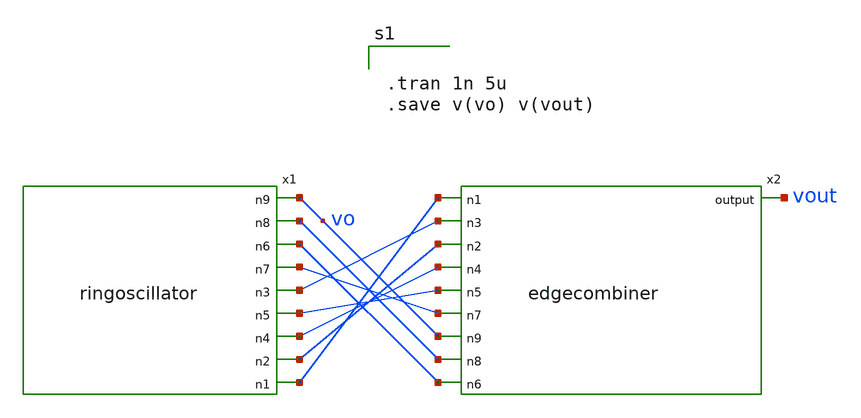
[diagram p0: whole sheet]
** sch_path: osccombiner.sch
**.subckt osccombiner
x2 vout net1 net3 net2 net4 net5 net7 vo net8 net6 edgecombiner
x1 vo net8 net6 net7 net3 net5 net4 net2 net1 ringoscillator
**** begin user architecture code


.tran 1n 5u
.save v(vo) v(vout)


*.lib ~/open_pdks/sky130/sky130A/libs.tech/ngspice/sky130.lib.spice tt
.param mc_mm_switch=0
.param mc_pr_switch=0

.include ~/open_pdks/sky130/sky130A/libs.tech/ngspice/corners/tt/nonfet.spice


*model
.include ~/open_pdks/sky130/sky130A/libs.tech/ngspice/all.spice

*mosfet
.include ~/open_pdks/sky130/sky130A/libs.ref/sky130_fd_pr/spice/sky130_fd_pr__pfet_01v8__tt.corner.spice
.inclued ~/open_pdks/sky130/sky130A/libs.ref/sky130_fd_pr/spice/sky130_fd_pr__nfet_01v8__tt.corner.spice

*mismatch parameters
.include ~/open_pdks/sky130/sky130A/libs.ref/sky130_fd_pr/spice/sky130_fd_pr__pfet_01v8__mismatch.corner.spice
.include ~/open_pdks/sky130/sky130A/libs.ref/sky130_fd_pr/spice/sky130_fd_pr__nfet_01v8__mismatch.corner.spice

**** end user architecture code
**.ends

* expanding   symbol:  /home/cegrahul/Downloads/edgecombiner.sym # of pins=10
** sym_path: edgecombiner.sym
** sch_path: edgecombiner.sch
.subckt edgecombiner output n1 n3 n2 n4 n5 n7 n9 n8 n6
*.ipin n1
*.ipin n2
*.ipin n3
*.ipin n4
*.ipin n5
*.ipin n6
*.ipin n7
*.ipin n8
*.ipin n9
*.opin output
XM3 v4 n5 VDD VDD sky130_fd_pr__pfet_01v8 L=0.15 W=1.68 nf=1 ad='int((nf+1)/2) * W/nf * 0.29' as='int((nf+2)/2) * W/nf * 0.29'
+ pd='2*int((nf+1)/2) * (W/nf + 0.29)' ps='2*int((nf+2)/2) * (W/nf + 0.29)' nrd='0.29 / W' nrs='0.29 / W'
+ sa=0 sb=0 sd=0 mult=1 m=1
XM4 v4 n4 VDD VDD sky130_fd_pr__pfet_01v8 L=0.15 W=1.68 nf=1 ad='int((nf+1)/2) * W/nf * 0.29' as='int((nf+2)/2) * W/nf * 0.29'
+ pd='2*int((nf+1)/2) * (W/nf + 0.29)' ps='2*int((nf+2)/2) * (W/nf + 0.29)' nrd='0.29 / W' nrs='0.29 / W'
+ sa=0 sb=0 sd=0 mult=1 m=1
XM5 v5 n5 net2 GND sky130_fd_pr__nfet_01v8 L=0.15 W=0.74 nf=1 ad='int((nf+1)/2) * W/nf * 0.29' as='int((nf+2)/2) * W/nf * 0.29'
+ pd='2*int((nf+1)/2) * (W/nf + 0.29)' ps='2*int((nf+2)/2) * (W/nf + 0.29)' nrd='0.29 / W' nrs='0.29 / W'
+ sa=0 sb=0 sd=0 mult=1 m=1
XM6 net2 n6 GND GND sky130_fd_pr__nfet_01v8 L=0.15 W=0.74 nf=1 ad='int((nf+1)/2) * W/nf * 0.29' as='int((nf+2)/2) * W/nf * 0.29'
+ pd='2*int((nf+1)/2) * (W/nf + 0.29)' ps='2*int((nf+2)/2) * (W/nf + 0.29)' nrd='0.29 / W' nrs='0.29 / W'
+ sa=0 sb=0 sd=0 mult=1 m=1
XM7 v5 n6 VDD VDD sky130_fd_pr__pfet_01v8 L=0.15 W=1.68 nf=1 ad='int((nf+1)/2) * W/nf * 0.29' as='int((nf+2)/2) * W/nf * 0.29'
+ pd='2*int((nf+1)/2) * (W/nf + 0.29)' ps='2*int((nf+2)/2) * (W/nf + 0.29)' nrd='0.29 / W' nrs='0.29 / W'
+ sa=0 sb=0 sd=0 mult=1 m=1
XM8 v5 n5 VDD VDD sky130_fd_pr__pfet_01v8 L=0.15 W=1.68 nf=1 ad='int((nf+1)/2) * W/nf * 0.29' as='int((nf+2)/2) * W/nf * 0.29'
+ pd='2*int((nf+1)/2) * (W/nf + 0.29)' ps='2*int((nf+2)/2) * (W/nf + 0.29)' nrd='0.29 / W' nrs='0.29 / W'
+ sa=0 sb=0 sd=0 mult=1 m=1
XM9 v6 n6 net3 GND sky130_fd_pr__nfet_01v8 L=0.15 W=0.74 nf=1 ad='int((nf+1)/2) * W/nf * 0.29' as='int((nf+2)/2) * W/nf * 0.29'
+ pd='2*int((nf+1)/2) * (W/nf + 0.29)' ps='2*int((nf+2)/2) * (W/nf + 0.29)' nrd='0.29 / W' nrs='0.29 / W'
+ sa=0 sb=0 sd=0 mult=1 m=1
XM10 net3 n7 GND GND sky130_fd_pr__nfet_01v8 L=0.15 W=0.74 nf=1 ad='int((nf+1)/2) * W/nf * 0.29' as='int((nf+2)/2) * W/nf * 0.29'
+ pd='2*int((nf+1)/2) * (W/nf + 0.29)' ps='2*int((nf+2)/2) * (W/nf + 0.29)' nrd='0.29 / W' nrs='0.29 / W'
+ sa=0 sb=0 sd=0 mult=1 m=1
XM11 v6 n7 VDD VDD sky130_fd_pr__pfet_01v8 L=0.15 W=1.68 nf=1 ad='int((nf+1)/2) * W/nf * 0.29' as='int((nf+2)/2) * W/nf * 0.29'
+ pd='2*int((nf+1)/2) * (W/nf + 0.29)' ps='2*int((nf+2)/2) * (W/nf + 0.29)' nrd='0.29 / W' nrs='0.29 / W'
+ sa=0 sb=0 sd=0 mult=1 m=1
XM12 v6 n6 VDD VDD sky130_fd_pr__pfet_01v8 L=0.15 W=1.68 nf=1 ad='int((nf+1)/2) * W/nf * 0.29' as='int((nf+2)/2) * W/nf * 0.29'
+ pd='2*int((nf+1)/2) * (W/nf + 0.29)' ps='2*int((nf+2)/2) * (W/nf + 0.29)' nrd='0.29 / W' nrs='0.29 / W'
+ sa=0 sb=0 sd=0 mult=1 m=1
XM13 v7 n7 net4 GND sky130_fd_pr__nfet_01v8 L=0.15 W=0.74 nf=1 ad='int((nf+1)/2) * W/nf * 0.29' as='int((nf+2)/2) * W/nf * 0.29'
+ pd='2*int((nf+1)/2) * (W/nf + 0.29)' ps='2*int((nf+2)/2) * (W/nf + 0.29)' nrd='0.29 / W' nrs='0.29 / W'
+ sa=0 sb=0 sd=0 mult=1 m=1
XM14 net4 n8 GND GND sky130_fd_pr__nfet_01v8 L=0.15 W=0.74 nf=1 ad='int((nf+1)/2) * W/nf * 0.29' as='int((nf+2)/2) * W/nf * 0.29'
+ pd='2*int((nf+1)/2) * (W/nf + 0.29)' ps='2*int((nf+2)/2) * (W/nf + 0.29)' nrd='0.29 / W' nrs='0.29 / W'
+ sa=0 sb=0 sd=0 mult=1 m=1
XM15 v7 n8 VDD VDD sky130_fd_pr__pfet_01v8 L=0.15 W=1.68 nf=1 ad='int((nf+1)/2) * W/nf * 0.29' as='int((nf+2)/2) * W/nf * 0.29'
+ pd='2*int((nf+1)/2) * (W/nf + 0.29)' ps='2*int((nf+2)/2) * (W/nf + 0.29)' nrd='0.29 / W' nrs='0.29 / W'
+ sa=0 sb=0 sd=0 mult=1 m=1
XM16 v7 n7 VDD VDD sky130_fd_pr__pfet_01v8 L=0.15 W=1.68 nf=1 ad='int((nf+1)/2) * W/nf * 0.29' as='int((nf+2)/2) * W/nf * 0.29'
+ pd='2*int((nf+1)/2) * (W/nf + 0.29)' ps='2*int((nf+2)/2) * (W/nf + 0.29)' nrd='0.29 / W' nrs='0.29 / W'
+ sa=0 sb=0 sd=0 mult=1 m=1
XM17 v4 n4 net1 GND sky130_fd_pr__nfet_01v8 L=0.15 W=0.74 nf=1 ad='int((nf+1)/2) * W/nf * 0.29' as='int((nf+2)/2) * W/nf * 0.29'
+ pd='2*int((nf+1)/2) * (W/nf + 0.29)' ps='2*int((nf+2)/2) * (W/nf + 0.29)' nrd='0.29 / W' nrs='0.29 / W'
+ sa=0 sb=0 sd=0 mult=1 m=1
XM18 net1 n5 GND GND sky130_fd_pr__nfet_01v8 L=0.15 W=0.74 nf=1 ad='int((nf+1)/2) * W/nf * 0.29' as='int((nf+2)/2) * W/nf * 0.29'
+ pd='2*int((nf+1)/2) * (W/nf + 0.29)' ps='2*int((nf+2)/2) * (W/nf + 0.29)' nrd='0.29 / W' nrs='0.29 / W'
+ sa=0 sb=0 sd=0 mult=1 m=1
XM19 v4 n5 VDD VDD sky130_fd_pr__pfet_01v8 L=0.15 W=1.68 nf=1 ad='int((nf+1)/2) * W/nf * 0.29' as='int((nf+2)/2) * W/nf * 0.29'
+ pd='2*int((nf+1)/2) * (W/nf + 0.29)' ps='2*int((nf+2)/2) * (W/nf + 0.29)' nrd='0.29 / W' nrs='0.29 / W'
+ sa=0 sb=0 sd=0 mult=1 m=1
XM20 v4 n4 VDD VDD sky130_fd_pr__pfet_01v8 L=0.15 W=1.68 nf=1 ad='int((nf+1)/2) * W/nf * 0.29' as='int((nf+2)/2) * W/nf * 0.29'
+ pd='2*int((nf+1)/2) * (W/nf + 0.29)' ps='2*int((nf+2)/2) * (W/nf + 0.29)' nrd='0.29 / W' nrs='0.29 / W'
+ sa=0 sb=0 sd=0 mult=1 m=1
XM21 v8 n8 net5 GND sky130_fd_pr__nfet_01v8 L=0.15 W=0.74 nf=1 ad='int((nf+1)/2) * W/nf * 0.29' as='int((nf+2)/2) * W/nf * 0.29'
+ pd='2*int((nf+1)/2) * (W/nf + 0.29)' ps='2*int((nf+2)/2) * (W/nf + 0.29)' nrd='0.29 / W' nrs='0.29 / W'
+ sa=0 sb=0 sd=0 mult=1 m=1
XM22 net5 n9 GND GND sky130_fd_pr__nfet_01v8 L=0.15 W=0.74 nf=1 ad='int((nf+1)/2) * W/nf * 0.29' as='int((nf+2)/2) * W/nf * 0.29'
+ pd='2*int((nf+1)/2) * (W/nf + 0.29)' ps='2*int((nf+2)/2) * (W/nf + 0.29)' nrd='0.29 / W' nrs='0.29 / W'
+ sa=0 sb=0 sd=0 mult=1 m=1
XM23 v8 n9 VDD VDD sky130_fd_pr__pfet_01v8 L=0.15 W=1.68 nf=1 ad='int((nf+1)/2) * W/nf * 0.29' as='int((nf+2)/2) * W/nf * 0.29'
+ pd='2*int((nf+1)/2) * (W/nf + 0.29)' ps='2*int((nf+2)/2) * (W/nf + 0.29)' nrd='0.29 / W' nrs='0.29 / W'
+ sa=0 sb=0 sd=0 mult=1 m=1
XM24 v8 n8 VDD VDD sky130_fd_pr__pfet_01v8 L=0.15 W=1.68 nf=1 ad='int((nf+1)/2) * W/nf * 0.29' as='int((nf+2)/2) * W/nf * 0.29'
+ pd='2*int((nf+1)/2) * (W/nf + 0.29)' ps='2*int((nf+2)/2) * (W/nf + 0.29)' nrd='0.29 / W' nrs='0.29 / W'
+ sa=0 sb=0 sd=0 mult=1 m=1
XM25 v9 n9 net6 GND sky130_fd_pr__nfet_01v8 L=0.15 W=0.74 nf=1 ad='int((nf+1)/2) * W/nf * 0.29' as='int((nf+2)/2) * W/nf * 0.29'
+ pd='2*int((nf+1)/2) * (W/nf + 0.29)' ps='2*int((nf+2)/2) * (W/nf + 0.29)' nrd='0.29 / W' nrs='0.29 / W'
+ sa=0 sb=0 sd=0 mult=1 m=1
XM26 net6 n1 GND GND sky130_fd_pr__nfet_01v8 L=0.15 W=0.74 nf=1 ad='int((nf+1)/2) * W/nf * 0.29' as='int((nf+2)/2) * W/nf * 0.29'
+ pd='2*int((nf+1)/2) * (W/nf + 0.29)' ps='2*int((nf+2)/2) * (W/nf + 0.29)' nrd='0.29 / W' nrs='0.29 / W'
+ sa=0 sb=0 sd=0 mult=1 m=1
XM27 v9 n1 VDD VDD sky130_fd_pr__pfet_01v8 L=0.15 W=1.68 nf=1 ad='int((nf+1)/2) * W/nf * 0.29' as='int((nf+2)/2) * W/nf * 0.29'
+ pd='2*int((nf+1)/2) * (W/nf + 0.29)' ps='2*int((nf+2)/2) * (W/nf + 0.29)' nrd='0.29 / W' nrs='0.29 / W'
+ sa=0 sb=0 sd=0 mult=1 m=1
XM28 v9 n9 VDD VDD sky130_fd_pr__pfet_01v8 L=0.15 W=1.68 nf=1 ad='int((nf+1)/2) * W/nf * 0.29' as='int((nf+2)/2) * W/nf * 0.29'
+ pd='2*int((nf+1)/2) * (W/nf + 0.29)' ps='2*int((nf+2)/2) * (W/nf + 0.29)' nrd='0.29 / W' nrs='0.29 / W'
+ sa=0 sb=0 sd=0 mult=1 m=1
XM29 v3 n3 net7 GND sky130_fd_pr__nfet_01v8 L=0.15 W=0.74 nf=1 ad='int((nf+1)/2) * W/nf * 0.29' as='int((nf+2)/2) * W/nf * 0.29'
+ pd='2*int((nf+1)/2) * (W/nf + 0.29)' ps='2*int((nf+2)/2) * (W/nf + 0.29)' nrd='0.29 / W' nrs='0.29 / W'
+ sa=0 sb=0 sd=0 mult=1 m=1
XM30 net7 n4 GND GND sky130_fd_pr__nfet_01v8 L=0.15 W=0.74 nf=1 ad='int((nf+1)/2) * W/nf * 0.29' as='int((nf+2)/2) * W/nf * 0.29'
+ pd='2*int((nf+1)/2) * (W/nf + 0.29)' ps='2*int((nf+2)/2) * (W/nf + 0.29)' nrd='0.29 / W' nrs='0.29 / W'
+ sa=0 sb=0 sd=0 mult=1 m=1
XM31 v3 n4 VDD VDD sky130_fd_pr__pfet_01v8 L=0.15 W=1.68 nf=1 ad='int((nf+1)/2) * W/nf * 0.29' as='int((nf+2)/2) * W/nf * 0.29'
+ pd='2*int((nf+1)/2) * (W/nf + 0.29)' ps='2*int((nf+2)/2) * (W/nf + 0.29)' nrd='0.29 / W' nrs='0.29 / W'
+ sa=0 sb=0 sd=0 mult=1 m=1
XM32 v3 n3 VDD VDD sky130_fd_pr__pfet_01v8 L=0.15 W=1.68 nf=1 ad='int((nf+1)/2) * W/nf * 0.29' as='int((nf+2)/2) * W/nf * 0.29'
+ pd='2*int((nf+1)/2) * (W/nf + 0.29)' ps='2*int((nf+2)/2) * (W/nf + 0.29)' nrd='0.29 / W' nrs='0.29 / W'
+ sa=0 sb=0 sd=0 mult=1 m=1
XM33 v2 n2 net8 GND sky130_fd_pr__nfet_01v8 L=0.15 W=0.74 nf=1 ad='int((nf+1)/2) * W/nf * 0.29' as='int((nf+2)/2) * W/nf * 0.29'
+ pd='2*int((nf+1)/2) * (W/nf + 0.29)' ps='2*int((nf+2)/2) * (W/nf + 0.29)' nrd='0.29 / W' nrs='0.29 / W'
+ sa=0 sb=0 sd=0 mult=1 m=1
XM34 net8 n3 GND GND sky130_fd_pr__nfet_01v8 L=0.15 W=0.74 nf=1 ad='int((nf+1)/2) * W/nf * 0.29' as='int((nf+2)/2) * W/nf * 0.29'
+ pd='2*int((nf+1)/2) * (W/nf + 0.29)' ps='2*int((nf+2)/2) * (W/nf + 0.29)' nrd='0.29 / W' nrs='0.29 / W'
+ sa=0 sb=0 sd=0 mult=1 m=1
XM35 v2 n3 VDD VDD sky130_fd_pr__pfet_01v8 L=0.15 W=1.68 nf=1 ad='int((nf+1)/2) * W/nf * 0.29' as='int((nf+2)/2) * W/nf * 0.29'
+ pd='2*int((nf+1)/2) * (W/nf + 0.29)' ps='2*int((nf+2)/2) * (W/nf + 0.29)' nrd='0.29 / W' nrs='0.29 / W'
+ sa=0 sb=0 sd=0 mult=1 m=1
XM36 v2 n2 VDD VDD sky130_fd_pr__pfet_01v8 L=0.15 W=1.68 nf=1 ad='int((nf+1)/2) * W/nf * 0.29' as='int((nf+2)/2) * W/nf * 0.29'
+ pd='2*int((nf+1)/2) * (W/nf + 0.29)' ps='2*int((nf+2)/2) * (W/nf + 0.29)' nrd='0.29 / W' nrs='0.29 / W'
+ sa=0 sb=0 sd=0 mult=1 m=1
XM37 v1 n1 net9 GND sky130_fd_pr__nfet_01v8 L=0.15 W=0.74 nf=1 ad='int((nf+1)/2) * W/nf * 0.29' as='int((nf+2)/2) * W/nf * 0.29'
+ pd='2*int((nf+1)/2) * (W/nf + 0.29)' ps='2*int((nf+2)/2) * (W/nf + 0.29)' nrd='0.29 / W' nrs='0.29 / W'
+ sa=0 sb=0 sd=0 mult=1 m=1
XM38 net9 n2 GND GND sky130_fd_pr__nfet_01v8 L=0.15 W=0.74 nf=1 ad='int((nf+1)/2) * W/nf * 0.29' as='int((nf+2)/2) * W/nf * 0.29'
+ pd='2*int((nf+1)/2) * (W/nf + 0.29)' ps='2*int((nf+2)/2) * (W/nf + 0.29)' nrd='0.29 / W' nrs='0.29 / W'
+ sa=0 sb=0 sd=0 mult=1 m=1
XM39 v1 n2 VDD VDD sky130_fd_pr__pfet_01v8 L=0.15 W=1.68 nf=1 ad='int((nf+1)/2) * W/nf * 0.29' as='int((nf+2)/2) * W/nf * 0.29'
+ pd='2*int((nf+1)/2) * (W/nf + 0.29)' ps='2*int((nf+2)/2) * (W/nf + 0.29)' nrd='0.29 / W' nrs='0.29 / W'
+ sa=0 sb=0 sd=0 mult=1 m=1
XM40 v1 n1 VDD VDD sky130_fd_pr__pfet_01v8 L=0.15 W=1.68 nf=1 ad='int((nf+1)/2) * W/nf * 0.29' as='int((nf+2)/2) * W/nf * 0.29'
+ pd='2*int((nf+1)/2) * (W/nf + 0.29)' ps='2*int((nf+2)/2) * (W/nf + 0.29)' nrd='0.29 / W' nrs='0.29 / W'
+ sa=0 sb=0 sd=0 mult=1 m=1
V1 VDD GND 1.8
XM1 output v1 net10 GND sky130_fd_pr__nfet_01v8 L=0.15 W=0.74 nf=1 ad='int((nf+1)/2) * W/nf * 0.29' as='int((nf+2)/2) * W/nf * 0.29'
+ pd='2*int((nf+1)/2) * (W/nf + 0.29)' ps='2*int((nf+2)/2) * (W/nf + 0.29)' nrd='0.29 / W' nrs='0.29 / W'
+ sa=0 sb=0 sd=0 mult=1 m=1
XM2 net10 v2 net11 GND sky130_fd_pr__nfet_01v8 L=0.15 W=3 nf=1 ad='int((nf+1)/2) * W/nf * 0.29' as='int((nf+2)/2) * W/nf * 0.29'
+ pd='2*int((nf+1)/2) * (W/nf + 0.29)' ps='2*int((nf+2)/2) * (W/nf + 0.29)' nrd='0.29 / W' nrs='0.29 / W'
+ sa=0 sb=0 sd=0 mult=1 m=1
XM41 output v2 VDD VDD sky130_fd_pr__pfet_01v8 L=0.15 W=1.68 nf=1 ad='int((nf+1)/2) * W/nf * 0.29' as='int((nf+2)/2) * W/nf * 0.29'
+ pd='2*int((nf+1)/2) * (W/nf + 0.29)' ps='2*int((nf+2)/2) * (W/nf + 0.29)' nrd='0.29 / W' nrs='0.29 / W'
+ sa=0 sb=0 sd=0 mult=1 m=1
XM42 output v1 VDD VDD sky130_fd_pr__pfet_01v8 L=0.15 W=1.68 nf=1 ad='int((nf+1)/2) * W/nf * 0.29' as='int((nf+2)/2) * W/nf * 0.29'
+ pd='2*int((nf+1)/2) * (W/nf + 0.29)' ps='2*int((nf+2)/2) * (W/nf + 0.29)' nrd='0.29 / W' nrs='0.29 / W'
+ sa=0 sb=0 sd=0 mult=1 m=1
XM43 net11 v3 net12 GND sky130_fd_pr__nfet_01v8 L=0.15 W=3 nf=1 ad='int((nf+1)/2) * W/nf * 0.29' as='int((nf+2)/2) * W/nf * 0.29'
+ pd='2*int((nf+1)/2) * (W/nf + 0.29)' ps='2*int((nf+2)/2) * (W/nf + 0.29)' nrd='0.29 / W' nrs='0.29 / W'
+ sa=0 sb=0 sd=0 mult=1 m=1
XM44 net12 v4 net13 GND sky130_fd_pr__nfet_01v8 L=0.15 W=3 nf=1 ad='int((nf+1)/2) * W/nf * 0.29' as='int((nf+2)/2) * W/nf * 0.29'
+ pd='2*int((nf+1)/2) * (W/nf + 0.29)' ps='2*int((nf+2)/2) * (W/nf + 0.29)' nrd='0.29 / W' nrs='0.29 / W'
+ sa=0 sb=0 sd=0 mult=1 m=1
XM45 net13 v5 net14 GND sky130_fd_pr__nfet_01v8 L=0.15 W=3 nf=1 ad='int((nf+1)/2) * W/nf * 0.29' as='int((nf+2)/2) * W/nf * 0.29'
+ pd='2*int((nf+1)/2) * (W/nf + 0.29)' ps='2*int((nf+2)/2) * (W/nf + 0.29)' nrd='0.29 / W' nrs='0.29 / W'
+ sa=0 sb=0 sd=0 mult=1 m=1
XM46 net15 v7 net16 GND sky130_fd_pr__nfet_01v8 L=0.15 W=3 nf=1 ad='int((nf+1)/2) * W/nf * 0.29' as='int((nf+2)/2) * W/nf * 0.29'
+ pd='2*int((nf+1)/2) * (W/nf + 0.29)' ps='2*int((nf+2)/2) * (W/nf + 0.29)' nrd='0.29 / W' nrs='0.29 / W'
+ sa=0 sb=0 sd=0 mult=1 m=1
XM47 net14 v6 net15 GND sky130_fd_pr__nfet_01v8 L=0.15 W=3 nf=1 ad='int((nf+1)/2) * W/nf * 0.29' as='int((nf+2)/2) * W/nf * 0.29'
+ pd='2*int((nf+1)/2) * (W/nf + 0.29)' ps='2*int((nf+2)/2) * (W/nf + 0.29)' nrd='0.29 / W' nrs='0.29 / W'
+ sa=0 sb=0 sd=0 mult=1 m=1
XM48 net16 v8 net17 GND sky130_fd_pr__nfet_01v8 L=0.15 W=3 nf=1 ad='int((nf+1)/2) * W/nf * 0.29' as='int((nf+2)/2) * W/nf * 0.29'
+ pd='2*int((nf+1)/2) * (W/nf + 0.29)' ps='2*int((nf+2)/2) * (W/nf + 0.29)' nrd='0.29 / W' nrs='0.29 / W'
+ sa=0 sb=0 sd=0 mult=1 m=1
XM49 net17 v9 GND GND sky130_fd_pr__nfet_01v8 L=0.15 W=3 nf=1 ad='int((nf+1)/2) * W/nf * 0.29' as='int((nf+2)/2) * W/nf * 0.29'
+ pd='2*int((nf+1)/2) * (W/nf + 0.29)' ps='2*int((nf+2)/2) * (W/nf + 0.29)' nrd='0.29 / W' nrs='0.29 / W'
+ sa=0 sb=0 sd=0 mult=1 m=1
XM51 output v4 VDD VDD sky130_fd_pr__pfet_01v8 L=0.15 W=1.68 nf=1 ad='int((nf+1)/2) * W/nf * 0.29' as='int((nf+2)/2) * W/nf * 0.29'
+ pd='2*int((nf+1)/2) * (W/nf + 0.29)' ps='2*int((nf+2)/2) * (W/nf + 0.29)' nrd='0.29 / W' nrs='0.29 / W'
+ sa=0 sb=0 sd=0 mult=1 m=1
XM52 output v5 VDD VDD sky130_fd_pr__pfet_01v8 L=0.15 W=1.68 nf=1 ad='int((nf+1)/2) * W/nf * 0.29' as='int((nf+2)/2) * W/nf * 0.29'
+ pd='2*int((nf+1)/2) * (W/nf + 0.29)' ps='2*int((nf+2)/2) * (W/nf + 0.29)' nrd='0.29 / W' nrs='0.29 / W'
+ sa=0 sb=0 sd=0 mult=1 m=1
XM53 output v6 VDD VDD sky130_fd_pr__pfet_01v8 L=0.15 W=1.68 nf=1 ad='int((nf+1)/2) * W/nf * 0.29' as='int((nf+2)/2) * W/nf * 0.29'
+ pd='2*int((nf+1)/2) * (W/nf + 0.29)' ps='2*int((nf+2)/2) * (W/nf + 0.29)' nrd='0.29 / W' nrs='0.29 / W'
+ sa=0 sb=0 sd=0 mult=1 m=1
XM54 output v7 VDD VDD sky130_fd_pr__pfet_01v8 L=0.15 W=1.68 nf=1 ad='int((nf+1)/2) * W/nf * 0.29' as='int((nf+2)/2) * W/nf * 0.29'
+ pd='2*int((nf+1)/2) * (W/nf + 0.29)' ps='2*int((nf+2)/2) * (W/nf + 0.29)' nrd='0.29 / W' nrs='0.29 / W'
+ sa=0 sb=0 sd=0 mult=1 m=1
XM55 output v8 VDD VDD sky130_fd_pr__pfet_01v8 L=0.15 W=1.68 nf=1 ad='int((nf+1)/2) * W/nf * 0.29' as='int((nf+2)/2) * W/nf * 0.29'
+ pd='2*int((nf+1)/2) * (W/nf + 0.29)' ps='2*int((nf+2)/2) * (W/nf + 0.29)' nrd='0.29 / W' nrs='0.29 / W'
+ sa=0 sb=0 sd=0 mult=1 m=1
XM56 output v9 VDD VDD sky130_fd_pr__pfet_01v8 L=0.15 W=1.68 nf=1 ad='int((nf+1)/2) * W/nf * 0.29' as='int((nf+2)/2) * W/nf * 0.29'
+ pd='2*int((nf+1)/2) * (W/nf + 0.29)' ps='2*int((nf+2)/2) * (W/nf + 0.29)' nrd='0.29 / W' nrs='0.29 / W'
+ sa=0 sb=0 sd=0 mult=1 m=1
XM50 output v3 VDD VDD sky130_fd_pr__pfet_01v8 L=0.15 W=1.68 nf=1 ad='int((nf+1)/2) * W/nf * 0.29' as='int((nf+2)/2) * W/nf * 0.29'
+ pd='2*int((nf+1)/2) * (W/nf + 0.29)' ps='2*int((nf+2)/2) * (W/nf + 0.29)' nrd='0.29 / W' nrs='0.29 / W'
+ sa=0 sb=0 sd=0 mult=1 m=1
.ends


* expanding   symbol:  /home/cegrahul/Desktop/SSCS/ringoscillator.sym # of pins=9
** sym_path: ringoscillator.sym
** sch_path: ringoscillator.sch
.subckt ringoscillator n9 n8 n6 n7 n3 n5 n4 n2 n1
*.opin n1
*.opin n2
*.opin n3
*.opin n4
*.opin n5
*.opin n6
*.opin n8
*.opin n9
*.opin n7
XM1 net1 net5 net2 GND sky130_fd_pr__nfet_01v8 L=4 W=1 nf=1 ad='int((nf+1)/2) * W/nf * 0.29' as='int((nf+2)/2) * W/nf * 0.29'
+ pd='2*int((nf+1)/2) * (W/nf + 0.29)' ps='2*int((nf+2)/2) * (W/nf + 0.29)' nrd='0.29 / W' nrs='0.29 / W'
+ sa=0 sb=0 sd=0 mult=1 m=1
XM3 net1 net5 net3 net4 sky130_fd_pr__pfet_01v8 L=4 W=0.55 nf=1 ad='int((nf+1)/2) * W/nf * 0.29' as='int((nf+2)/2) * W/nf * 0.29'
+ pd='2*int((nf+1)/2) * (W/nf + 0.29)' ps='2*int((nf+2)/2) * (W/nf + 0.29)' nrd='0.29 / W' nrs='0.29 / W'
+ sa=0 sb=0 sd=0 mult=4 m=4
XM19 net2 net5 GND GND sky130_fd_pr__nfet_01v8 L=4 W=1 nf=1 ad='int((nf+1)/2) * W/nf * 0.29' as='int((nf+2)/2) * W/nf * 0.29'
+ pd='2*int((nf+1)/2) * (W/nf + 0.29)' ps='2*int((nf+2)/2) * (W/nf + 0.29)' nrd='0.29 / W' nrs='0.29 / W'
+ sa=0 sb=0 sd=0 mult=1 m=1
XM2 net6 net1 net7 GND sky130_fd_pr__nfet_01v8 L=4 W=1 nf=1 ad='int((nf+1)/2) * W/nf * 0.29' as='int((nf+2)/2) * W/nf * 0.29'
+ pd='2*int((nf+1)/2) * (W/nf + 0.29)' ps='2*int((nf+2)/2) * (W/nf + 0.29)' nrd='0.29 / W' nrs='0.29 / W'
+ sa=0 sb=0 sd=0 mult=1 m=1
XM4 net6 net1 net8 net4 sky130_fd_pr__pfet_01v8 L=4 W=0.55 nf=1 ad='int((nf+1)/2) * W/nf * 0.29' as='int((nf+2)/2) * W/nf * 0.29'
+ pd='2*int((nf+1)/2) * (W/nf + 0.29)' ps='2*int((nf+2)/2) * (W/nf + 0.29)' nrd='0.29 / W' nrs='0.29 / W'
+ sa=0 sb=0 sd=0 mult=4 m=4
XM5 net7 net1 GND GND sky130_fd_pr__nfet_01v8 L=4 W=1 nf=1 ad='int((nf+1)/2) * W/nf * 0.29' as='int((nf+2)/2) * W/nf * 0.29'
+ pd='2*int((nf+1)/2) * (W/nf + 0.29)' ps='2*int((nf+2)/2) * (W/nf + 0.29)' nrd='0.29 / W' nrs='0.29 / W'
+ sa=0 sb=0 sd=0 mult=1 m=1
XM6 net9 net6 net10 GND sky130_fd_pr__nfet_01v8 L=4 W=1 nf=1 ad='int((nf+1)/2) * W/nf * 0.29' as='int((nf+2)/2) * W/nf * 0.29'
+ pd='2*int((nf+1)/2) * (W/nf + 0.29)' ps='2*int((nf+2)/2) * (W/nf + 0.29)' nrd='0.29 / W' nrs='0.29 / W'
+ sa=0 sb=0 sd=0 mult=1 m=1
XM7 net9 net6 net11 net4 sky130_fd_pr__pfet_01v8 L=4 W=0.55 nf=1 ad='int((nf+1)/2) * W/nf * 0.29' as='int((nf+2)/2) * W/nf * 0.29'
+ pd='2*int((nf+1)/2) * (W/nf + 0.29)' ps='2*int((nf+2)/2) * (W/nf + 0.29)' nrd='0.29 / W' nrs='0.29 / W'
+ sa=0 sb=0 sd=0 mult=4 m=4
XM8 net10 net6 GND GND sky130_fd_pr__nfet_01v8 L=4 W=1 nf=1 ad='int((nf+1)/2) * W/nf * 0.29' as='int((nf+2)/2) * W/nf * 0.29'
+ pd='2*int((nf+1)/2) * (W/nf + 0.29)' ps='2*int((nf+2)/2) * (W/nf + 0.29)' nrd='0.29 / W' nrs='0.29 / W'
+ sa=0 sb=0 sd=0 mult=1 m=1
XM9 net12 net9 net13 GND sky130_fd_pr__nfet_01v8 L=4 W=1 nf=1 ad='int((nf+1)/2) * W/nf * 0.29' as='int((nf+2)/2) * W/nf * 0.29'
+ pd='2*int((nf+1)/2) * (W/nf + 0.29)' ps='2*int((nf+2)/2) * (W/nf + 0.29)' nrd='0.29 / W' nrs='0.29 / W'
+ sa=0 sb=0 sd=0 mult=1 m=1
XM10 net12 net9 net14 net4 sky130_fd_pr__pfet_01v8 L=4 W=0.55 nf=1 ad='int((nf+1)/2) * W/nf * 0.29' as='int((nf+2)/2) * W/nf * 0.29'
+ pd='2*int((nf+1)/2) * (W/nf + 0.29)' ps='2*int((nf+2)/2) * (W/nf + 0.29)' nrd='0.29 / W' nrs='0.29 / W'
+ sa=0 sb=0 sd=0 mult=4 m=4
XM11 net13 net9 GND GND sky130_fd_pr__nfet_01v8 L=4 W=1 nf=1 ad='int((nf+1)/2) * W/nf * 0.29' as='int((nf+2)/2) * W/nf * 0.29'
+ pd='2*int((nf+1)/2) * (W/nf + 0.29)' ps='2*int((nf+2)/2) * (W/nf + 0.29)' nrd='0.29 / W' nrs='0.29 / W'
+ sa=0 sb=0 sd=0 mult=1 m=1
XM12 net15 net12 net16 GND sky130_fd_pr__nfet_01v8 L=4 W=1 nf=1 ad='int((nf+1)/2) * W/nf * 0.29' as='int((nf+2)/2) * W/nf * 0.29'
+ pd='2*int((nf+1)/2) * (W/nf + 0.29)' ps='2*int((nf+2)/2) * (W/nf + 0.29)' nrd='0.29 / W' nrs='0.29 / W'
+ sa=0 sb=0 sd=0 mult=1 m=1
XM13 net15 net12 net17 net4 sky130_fd_pr__pfet_01v8 L=4 W=0.55 nf=1 ad='int((nf+1)/2) * W/nf * 0.29'
+ as='int((nf+2)/2) * W/nf * 0.29' pd='2*int((nf+1)/2) * (W/nf + 0.29)' ps='2*int((nf+2)/2) * (W/nf + 0.29)'
+ nrd='0.29 / W' nrs='0.29 / W' sa=0 sb=0 sd=0 mult=4 m=4
XM14 net16 net12 GND GND sky130_fd_pr__nfet_01v8 L=4 W=1 nf=1 ad='int((nf+1)/2) * W/nf * 0.29' as='int((nf+2)/2) * W/nf * 0.29'
+ pd='2*int((nf+1)/2) * (W/nf + 0.29)' ps='2*int((nf+2)/2) * (W/nf + 0.29)' nrd='0.29 / W' nrs='0.29 / W'
+ sa=0 sb=0 sd=0 mult=1 m=1
XM15 net18 net15 net19 GND sky130_fd_pr__nfet_01v8 L=4 W=1 nf=1 ad='int((nf+1)/2) * W/nf * 0.29' as='int((nf+2)/2) * W/nf * 0.29'
+ pd='2*int((nf+1)/2) * (W/nf + 0.29)' ps='2*int((nf+2)/2) * (W/nf + 0.29)' nrd='0.29 / W' nrs='0.29 / W'
+ sa=0 sb=0 sd=0 mult=1 m=1
XM16 net18 net15 net20 net4 sky130_fd_pr__pfet_01v8 L=4 W=0.55 nf=1 ad='int((nf+1)/2) * W/nf * 0.29'
+ as='int((nf+2)/2) * W/nf * 0.29' pd='2*int((nf+1)/2) * (W/nf + 0.29)' ps='2*int((nf+2)/2) * (W/nf + 0.29)'
+ nrd='0.29 / W' nrs='0.29 / W' sa=0 sb=0 sd=0 mult=4 m=4
XM17 net19 net15 GND GND sky130_fd_pr__nfet_01v8 L=4 W=1 nf=1 ad='int((nf+1)/2) * W/nf * 0.29' as='int((nf+2)/2) * W/nf * 0.29'
+ pd='2*int((nf+1)/2) * (W/nf + 0.29)' ps='2*int((nf+2)/2) * (W/nf + 0.29)' nrd='0.29 / W' nrs='0.29 / W'
+ sa=0 sb=0 sd=0 mult=1 m=1
XM18 net21 net18 net22 GND sky130_fd_pr__nfet_01v8 L=4 W=1 nf=1 ad='int((nf+1)/2) * W/nf * 0.29' as='int((nf+2)/2) * W/nf * 0.29'
+ pd='2*int((nf+1)/2) * (W/nf + 0.29)' ps='2*int((nf+2)/2) * (W/nf + 0.29)' nrd='0.29 / W' nrs='0.29 / W'
+ sa=0 sb=0 sd=0 mult=1 m=1
XM20 net21 net18 net23 net4 sky130_fd_pr__pfet_01v8 L=4 W=0.55 nf=1 ad='int((nf+1)/2) * W/nf * 0.29'
+ as='int((nf+2)/2) * W/nf * 0.29' pd='2*int((nf+1)/2) * (W/nf + 0.29)' ps='2*int((nf+2)/2) * (W/nf + 0.29)'
+ nrd='0.29 / W' nrs='0.29 / W' sa=0 sb=0 sd=0 mult=4 m=4
XM21 net22 net18 GND GND sky130_fd_pr__nfet_01v8 L=4 W=1 nf=1 ad='int((nf+1)/2) * W/nf * 0.29' as='int((nf+2)/2) * W/nf * 0.29'
+ pd='2*int((nf+1)/2) * (W/nf + 0.29)' ps='2*int((nf+2)/2) * (W/nf + 0.29)' nrd='0.29 / W' nrs='0.29 / W'
+ sa=0 sb=0 sd=0 mult=1 m=1
XM22 net24 net21 net25 GND sky130_fd_pr__nfet_01v8 L=4 W=1 nf=1 ad='int((nf+1)/2) * W/nf * 0.29' as='int((nf+2)/2) * W/nf * 0.29'
+ pd='2*int((nf+1)/2) * (W/nf + 0.29)' ps='2*int((nf+2)/2) * (W/nf + 0.29)' nrd='0.29 / W' nrs='0.29 / W'
+ sa=0 sb=0 sd=0 mult=1 m=1
XM23 net24 net21 net26 net4 sky130_fd_pr__pfet_01v8 L=4 W=0.55 nf=1 ad='int((nf+1)/2) * W/nf * 0.29'
+ as='int((nf+2)/2) * W/nf * 0.29' pd='2*int((nf+1)/2) * (W/nf + 0.29)' ps='2*int((nf+2)/2) * (W/nf + 0.29)'
+ nrd='0.29 / W' nrs='0.29 / W' sa=0 sb=0 sd=0 mult=4 m=4
XM24 net25 net21 GND GND sky130_fd_pr__nfet_01v8 L=4 W=1 nf=1 ad='int((nf+1)/2) * W/nf * 0.29' as='int((nf+2)/2) * W/nf * 0.29'
+ pd='2*int((nf+1)/2) * (W/nf + 0.29)' ps='2*int((nf+2)/2) * (W/nf + 0.29)' nrd='0.29 / W' nrs='0.29 / W'
+ sa=0 sb=0 sd=0 mult=1 m=1
XM25 net5 net24 net27 GND sky130_fd_pr__nfet_01v8 L=4 W=1 nf=1 ad='int((nf+1)/2) * W/nf * 0.29' as='int((nf+2)/2) * W/nf * 0.29'
+ pd='2*int((nf+1)/2) * (W/nf + 0.29)' ps='2*int((nf+2)/2) * (W/nf + 0.29)' nrd='0.29 / W' nrs='0.29 / W'
+ sa=0 sb=0 sd=0 mult=1 m=1
XM26 net5 net24 net28 net4 sky130_fd_pr__pfet_01v8 L=4 W=0.55 nf=1 ad='int((nf+1)/2) * W/nf * 0.29' as='int((nf+2)/2) * W/nf * 0.29'
+ pd='2*int((nf+1)/2) * (W/nf + 0.29)' ps='2*int((nf+2)/2) * (W/nf + 0.29)' nrd='0.29 / W' nrs='0.29 / W'
+ sa=0 sb=0 sd=0 mult=4 m=4
XM27 net27 net24 GND GND sky130_fd_pr__nfet_01v8 L=4 W=1 nf=1 ad='int((nf+1)/2) * W/nf * 0.29' as='int((nf+2)/2) * W/nf * 0.29'
+ pd='2*int((nf+1)/2) * (W/nf + 0.29)' ps='2*int((nf+2)/2) * (W/nf + 0.29)' nrd='0.29 / W' nrs='0.29 / W'
+ sa=0 sb=0 sd=0 mult=1 m=1
XM29 net3 net29 net4 net4 sky130_fd_pr__pfet_01v8 L=4 W=0.55 nf=1 ad='int((nf+1)/2) * W/nf * 0.29' as='int((nf+2)/2) * W/nf * 0.29'
+ pd='2*int((nf+1)/2) * (W/nf + 0.29)' ps='2*int((nf+2)/2) * (W/nf + 0.29)' nrd='0.29 / W' nrs='0.29 / W'
+ sa=0 sb=0 sd=0 mult=4 m=4
XM30 net8 net29 net4 net4 sky130_fd_pr__pfet_01v8 L=4 W=0.55 nf=1 ad='int((nf+1)/2) * W/nf * 0.29' as='int((nf+2)/2) * W/nf * 0.29'
+ pd='2*int((nf+1)/2) * (W/nf + 0.29)' ps='2*int((nf+2)/2) * (W/nf + 0.29)' nrd='0.29 / W' nrs='0.29 / W'
+ sa=0 sb=0 sd=0 mult=4 m=4
XM31 net11 net29 net4 net4 sky130_fd_pr__pfet_01v8 L=4 W=0.55 nf=1 ad='int((nf+1)/2) * W/nf * 0.29' as='int((nf+2)/2) * W/nf * 0.29'
+ pd='2*int((nf+1)/2) * (W/nf + 0.29)' ps='2*int((nf+2)/2) * (W/nf + 0.29)' nrd='0.29 / W' nrs='0.29 / W'
+ sa=0 sb=0 sd=0 mult=4 m=4
XM32 net14 net29 net4 net4 sky130_fd_pr__pfet_01v8 L=4 W=0.55 nf=1 ad='int((nf+1)/2) * W/nf * 0.29' as='int((nf+2)/2) * W/nf * 0.29'
+ pd='2*int((nf+1)/2) * (W/nf + 0.29)' ps='2*int((nf+2)/2) * (W/nf + 0.29)' nrd='0.29 / W' nrs='0.29 / W'
+ sa=0 sb=0 sd=0 mult=4 m=4
XM33 net17 net29 net4 net4 sky130_fd_pr__pfet_01v8 L=4 W=0.55 nf=1 ad='int((nf+1)/2) * W/nf * 0.29' as='int((nf+2)/2) * W/nf * 0.29'
+ pd='2*int((nf+1)/2) * (W/nf + 0.29)' ps='2*int((nf+2)/2) * (W/nf + 0.29)' nrd='0.29 / W' nrs='0.29 / W'
+ sa=0 sb=0 sd=0 mult=4 m=4
XM34 net20 net29 net4 net4 sky130_fd_pr__pfet_01v8 L=4 W=0.55 nf=1 ad='int((nf+1)/2) * W/nf * 0.29' as='int((nf+2)/2) * W/nf * 0.29'
+ pd='2*int((nf+1)/2) * (W/nf + 0.29)' ps='2*int((nf+2)/2) * (W/nf + 0.29)' nrd='0.29 / W' nrs='0.29 / W'
+ sa=0 sb=0 sd=0 mult=4 m=4
XM35 net23 net29 net4 net4 sky130_fd_pr__pfet_01v8 L=4 W=0.55 nf=1 ad='int((nf+1)/2) * W/nf * 0.29' as='int((nf+2)/2) * W/nf * 0.29'
+ pd='2*int((nf+1)/2) * (W/nf + 0.29)' ps='2*int((nf+2)/2) * (W/nf + 0.29)' nrd='0.29 / W' nrs='0.29 / W'
+ sa=0 sb=0 sd=0 mult=4 m=4
XM36 net26 net29 net4 net4 sky130_fd_pr__pfet_01v8 L=4 W=0.55 nf=1 ad='int((nf+1)/2) * W/nf * 0.29' as='int((nf+2)/2) * W/nf * 0.29'
+ pd='2*int((nf+1)/2) * (W/nf + 0.29)' ps='2*int((nf+2)/2) * (W/nf + 0.29)' nrd='0.29 / W' nrs='0.29 / W'
+ sa=0 sb=0 sd=0 mult=4 m=4
XM37 net28 net29 net4 net4 sky130_fd_pr__pfet_01v8 L=4 W=0.55 nf=1 ad='int((nf+1)/2) * W/nf * 0.29' as='int((nf+2)/2) * W/nf * 0.29'
+ pd='2*int((nf+1)/2) * (W/nf + 0.29)' ps='2*int((nf+2)/2) * (W/nf + 0.29)' nrd='0.29 / W' nrs='0.29 / W'
+ sa=0 sb=0 sd=0 mult=4 m=4
V3 net4 GND 1.8
V4 net29 GND 0.625
X1 net1 n1 inverter
X2 net6 n2 inverter
X3 net9 n3 inverter
X4 net12 n4 inverter
X5 net15 n5 inverter
X6 net18 n6 inverter
X7 net21 n7 inverter
X8 net24 n8 inverter
X9 net5 n9 inverter
.ends


* expanding   symbol:  /home/cegrahul/Desktop/SSCS/inverter.sym # of pins=2
** sym_path: inverter.sym
** sch_path: inverter.sch
.subckt inverter vin vout
*.ipin vin
*.opin vout
XM2 vout vin net1 net1 sky130_fd_pr__pfet_01v8 L=0.15 W=1.68 nf=1 ad='int((nf+1)/2) * W/nf * 0.29' as='int((nf+2)/2) * W/nf * 0.29'
+ pd='2*int((nf+1)/2) * (W/nf + 0.29)' ps='2*int((nf+2)/2) * (W/nf + 0.29)' nrd='0.29 / W' nrs='0.29 / W'
+ sa=0 sb=0 sd=0 mult=1 m=1
XM3 vout vin GND GND sky130_fd_pr__nfet_01v8 L=0.15 W=0.36 nf=1 ad='int((nf+1)/2) * W/nf * 0.29' as='int((nf+2)/2) * W/nf * 0.29'
+ pd='2*int((nf+1)/2) * (W/nf + 0.29)' ps='2*int((nf+2)/2) * (W/nf + 0.29)' nrd='0.29 / W' nrs='0.29 / W'
+ sa=0 sb=0 sd=0 mult=1 m=1
V3 net1 GND 1.8
.ends

.GLOBAL VDD
.GLOBAL GND
.end
